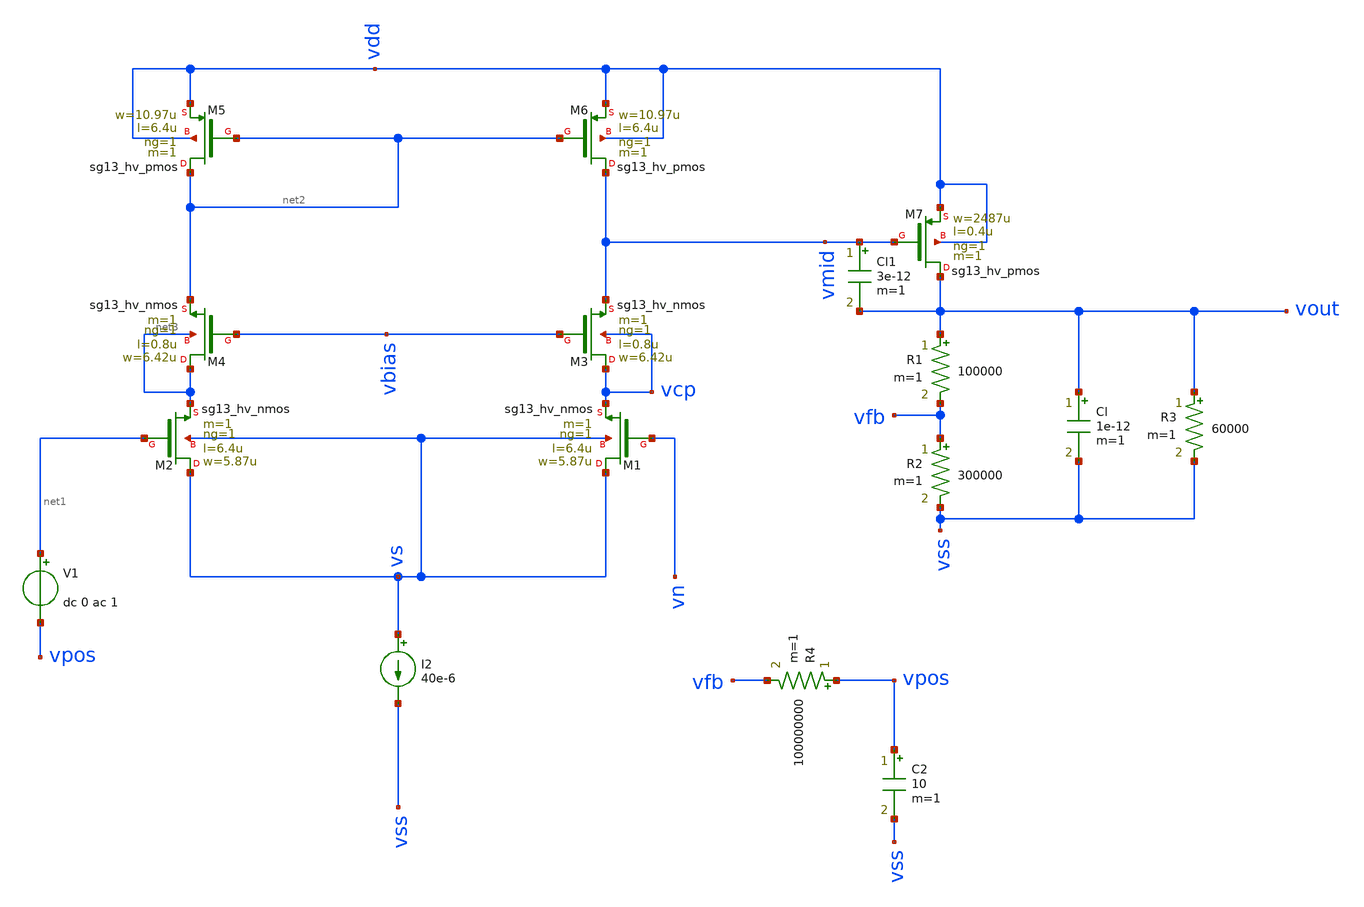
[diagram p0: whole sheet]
** sch_path: test/Tesis_notebooks/xschem/ldo_ol_sim_ihp_cc.sch
**.subckt ldo_ol_sim_ihp_cc
R1 vout vfb 100000 m=1
R2 vfb vss 300000 m=1
Cl vout vss 1e-12 m=1
R3 vout vss 60000 m=1
XM6 vmid net2 vdd vdd sg13_hv_pmos w=10.97u l=6.4u ng=1 m=1 mm_ok=1
I2 vs vss 40e-6
XM1 vs vn vcp vs sg13_hv_nmos w=5.87u l=6.4u ng=1 m=1 mm_ok=1
XM2 vs net1 net3 vs sg13_hv_nmos w=5.87u l=6.4u ng=1 m=1 mm_ok=1
XM3 vcp vbias vmid vcp sg13_hv_nmos w=6.42u l=0.8u ng=1 m=1 mm_ok=1
XM4 net3 vbias net2 net3 sg13_hv_nmos w=6.42u l=0.8u ng=1 m=1 mm_ok=1
XM5 net2 net2 vdd vdd sg13_hv_pmos w=10.97u l=6.4u ng=1 m=1 mm_ok=1
XM7 vout vmid vdd vdd sg13_hv_pmos w=2487u l=0.4u ng=1 m=1 mm_ok=1
R4 vpos vfb 100000000 m=1
C2 vpos vss 10 m=1
V1 net1 vpos dc 0 ac 1
Cl1 vmid vout 3e-12 m=1
**** begin user architecture code



.lib /opt/pdks/ihp-sg13g2/libs.tech/ngspice/models/cornerMOShv.lib mos_tt

Vref vn 0 1.35
Vdd vdd 0 3.3
Vss vss 0 0
Vbias vbias 0 2.2

.control
ac dec 10 1 100G
plot vdb(vout)
plot phase(vout)*180/PI
op
print vout vmid vcp vfb vs
.endc



**** end user architecture code
**.ends
.end
